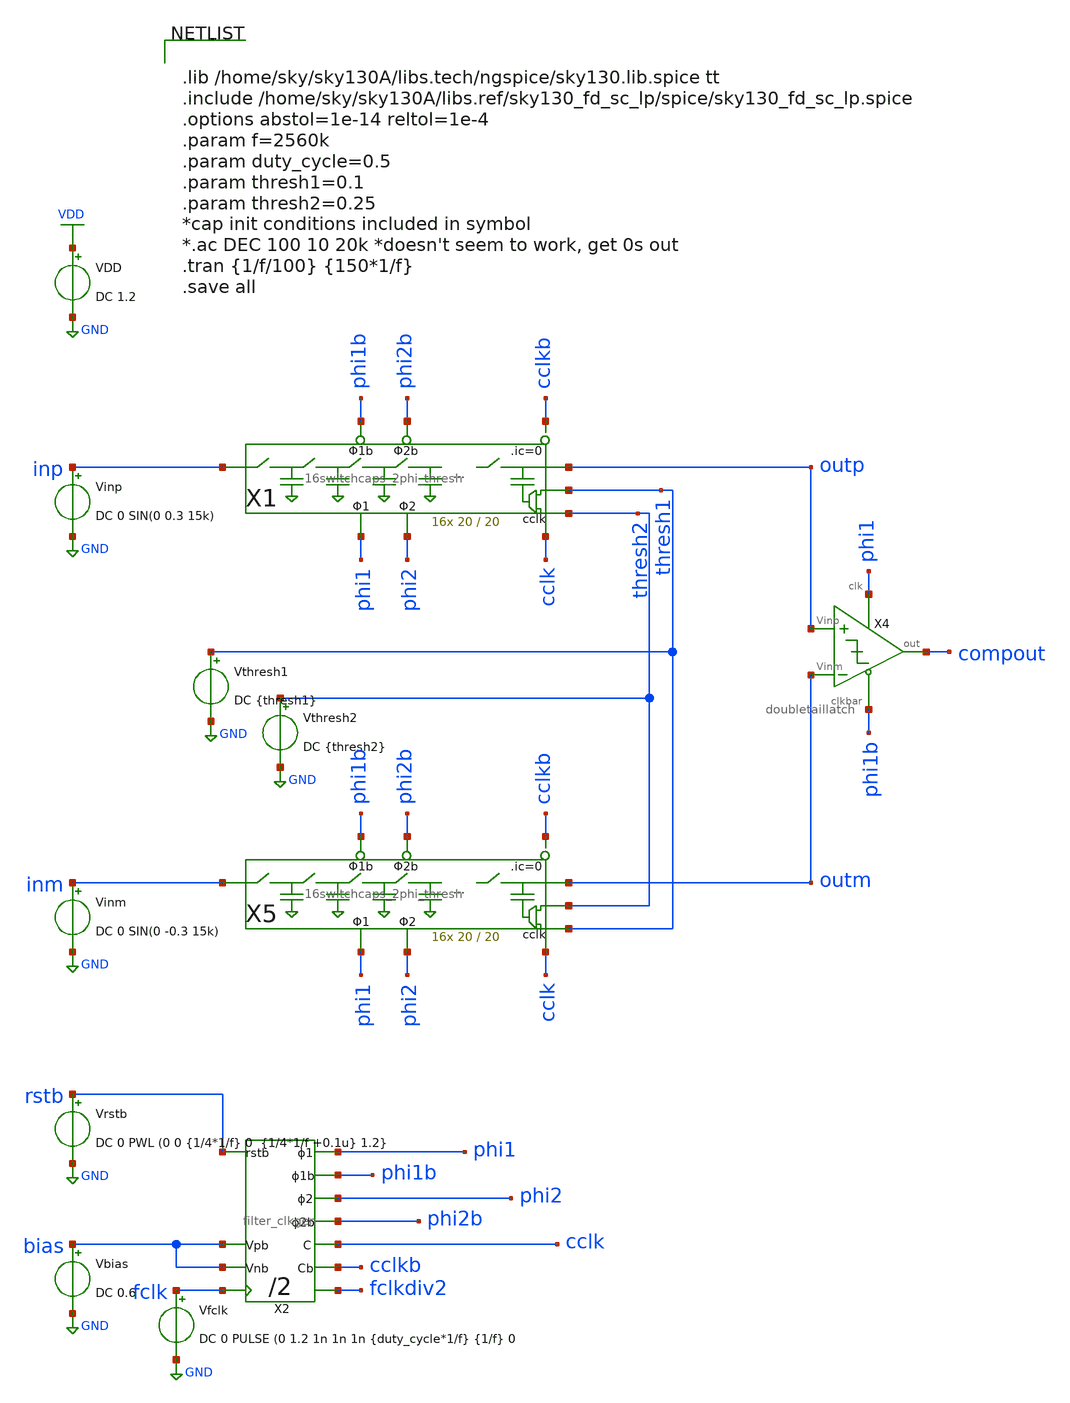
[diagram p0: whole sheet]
** sch_path: xschem/comparator/2switchcaps_thresh_diff_tb.sch
**.subckt 2switchcaps_thresh_diff_tb
Vinp inp GND DC 0 SIN(0 0.3 15k)
VDD VDD GND DC 1.2
Vfclk fclk GND DC 0 PULSE (0 1.2 1n 1n 1n {duty_cycle*1/f} {1/f} 0
X2 rstb fclk phi2b phi2 phi1b phi1 cclkb cclk fclkdiv2 bias bias filter_clkgen
Vbias bias GND DC 0.6
Vthresh1 thresh1 GND DC {thresh1}
Vthresh2 thresh2 GND DC {thresh2}
Vrstb rstb GND DC 0 PWL (0 0 {1/4*1/f} 0 {1/4*1/f +0.1u} 1.2}
Vinm inm GND DC 0 SIN(0 -0.3 15k)
X4 outp outm compout phi1 phi1b doubletaillatch
X5 inm outm phi1 phi1b phi2 phi2b cclk thresh2 thresh1 cclkb 16switchcaps_2phi_thresh W=20 L=20
X1 inp outp phi1 phi1b phi2 phi2b cclk thresh1 thresh2 cclkb 16switchcaps_2phi_thresh W=20 L=20
**** begin user architecture code


.lib /home/sky/sky130A/libs.tech/ngspice/sky130.lib.spice tt
.include /home/sky/sky130A/libs.ref/sky130_fd_sc_lp/spice/sky130_fd_sc_lp.spice
.options abstol=1e-14 reltol=1e-4
.param f=2560k
.param duty_cycle=0.5
.param thresh1=0.1
.param thresh2=0.25
*cap init conditions included in symbol
*.ac DEC 100 10 20k *doesn't seem to work, get 0s out
.tran {1/f/100} {150*1/f}
.save all


**** end user architecture code
**.ends
.GLOBAL GND
.GLOBAL VDD
.end
